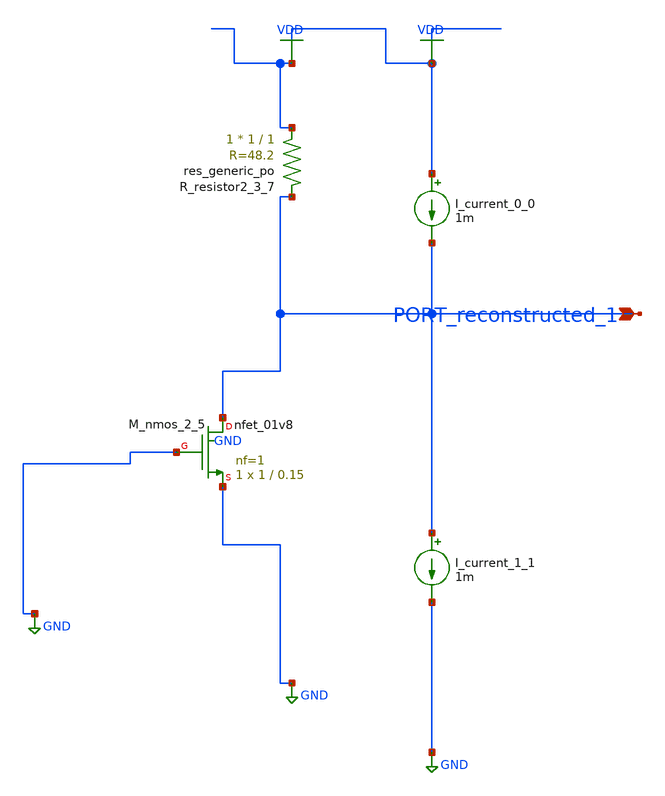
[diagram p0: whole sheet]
** sch_path: schematics/AMSNet/438.sch
**.subckt 438 PORT_reconstructed_1
*.ipin PORT_reconstructed_1
I_current_0_0 VDD PORT_reconstructed_1 1m
I_current_1_1 PORT_reconstructed_1 GND 1m
XM_nmos_2_5 PORT_reconstructed_1 GND GND GND sky130_fd_pr__nfet_01v8 L=0.15 W=1 nf=1 ad='int((1 + 1)/2) * 1 / 1 * 0.29'
+ as='int((1 + 2)/2) * 1 / 1 * 0.29' pd='2*int((1 + 1)/2) * (1 / 1 + 0.29)' ps='2*int((1 + 2)/2) * (1 / 1 + 0.29)'
+ nrd='0.29 / 1 ' nrs='0.29 / 1 ' sa=0 sb=0 sd=0 mult=1 m=1
XR_resistor2_3_7 VDD PORT_reconstructed_1 sky130_fd_pr__res_generic_po W=1 L=1 m=1
**.ends
.GLOBAL GND
.GLOBAL VDD
.end
